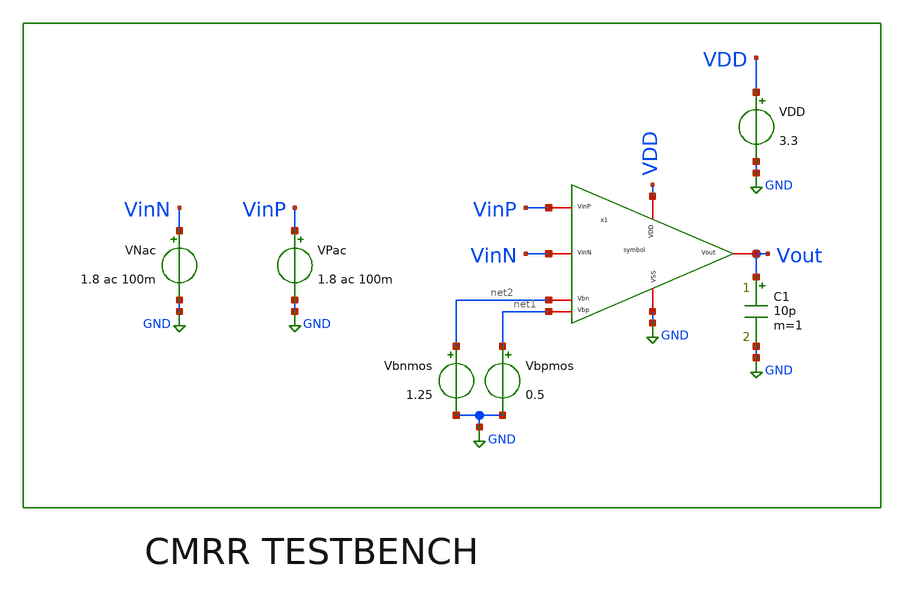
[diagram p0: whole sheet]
** sch_path: v2_bmr_bias/CMRRsim.sch
**.subckt CMRRsim
x1 VDD net1 VinP VinN Vout net2 GND symbol
VPac VinP GND 1.8 ac 100m
VNac VinN GND 1.8 ac 100m
Vbnmos net2 GND 1.25
Vbpmos net1 GND 0.5
VDD VDD GND 3.3
C1 Vout GND 10p m=1
**** begin user architecture code


.control
close all
destroy all

ac dec 20 1 500Meg
let gain_cm_db = db(Vout/VinP)
meas ac acm_dc_gain find gain_cm_db at=1

alter VNac ac = -100m
ac dec 20 1 200G
let VinDiff = v(VinP) - v(VinN)
let gain_dm_db = db(Vout/VinDiff)
meas ac adm_dc_gain find gain_dm_db at=1

let cmrr_dc   = adm_dc_gain - ac1.acm_dc_gain
let cmrr_full = gain_dm_db  - ac1.gain_cm_db

echo
echo '================ CMRR RESULTS ================'
print adm_dc_gain
print ac1.acm_dc_gain
print cmrr_dc
echo '================================================'

* --- plots ---
plot ac1.gain_cm_db gain_dm_db ylabel 'Gain (dB)' xlog title 'Common-Mode vs Differential Gain'
plot cmrr_full ylabel 'CMRR (dB)' xlog title 'CMRR vs Frequency'

.endc


**** end user architecture code
**.ends

* expanding   symbol:  /foss/designs/FOLDED/symbol.sym # of pins=7
** sym_path: v2_bmr_bias/symbol.sym
** sch_path: v2_bmr_bias/symbol.sch
.subckt symbol VDD Vbp VinP VinN Vout Vbn VSS
*.iopin Vbn
*.iopin Vbp
*.iopin VinP
*.iopin VinN
*.iopin Vout
*.iopin VDD
*.iopin VSS
XM1 net10 VinP net1 VSS sg13_hv_nmos w=7u l=1u ng=1 m=4 mm_ok=1
XM2 net9 VinN net1 VSS sg13_hv_nmos w=7u l=1u ng=1 m=4 mm_ok=1
XM3 net1 net3 VSS VSS sg13_hv_nmos w=3.75u l=1u ng=1 m=4 mm_ok=1
XM4 net10 net5 VDD VDD sg13_hv_pmos w=3.5u l=1u ng=1 m=4 mm_ok=1
XM5 net9 net5 VDD VDD sg13_hv_pmos w=3.5u l=1u ng=1 m=4 mm_ok=1
XM6 net2 Vbp net10 VDD sg13_hv_pmos w=4u l=1u ng=1 m=3 mm_ok=1
XM7 Vout Vbp net9 VDD sg13_hv_pmos w=4u l=1u ng=1 m=3 mm_ok=1
XM8 net2 Vbn net11 VSS sg13_hv_nmos w=7u l=1u ng=1 m=1 mm_ok=1
XM9 Vout Vbn net12 VSS sg13_hv_nmos w=7u l=1u ng=1 m=1 mm_ok=1
XM10 net11 net2 VSS VSS sg13_hv_nmos w=7u l=1u ng=1 m=1 mm_ok=1
XM11 net12 net2 VSS VSS sg13_hv_nmos w=7u l=1u ng=1 m=1 mm_ok=1
**** begin user architecture code



.lib cornerMOShv.lib mos_tt



**** end user architecture code
XM25 net3 net5 VDD VDD sg13_hv_pmos w=3.5u l=1u ng=1 m=1 mm_ok=1
XM12 net3 net3 VSS VSS sg13_hv_nmos w=3.75u l=1u ng=1 m=1 mm_ok=1
R1 net7 VSS 8.64k m=1
XM14 net8 net6 net7 VSS sg13_hv_nmos w=15u l=1u ng=2 m=1 mm_ok=1
XM15 net6 net6 VSS VSS sg13_hv_nmos w=3.75u l=1u ng=1 m=1 mm_ok=1
XM17 net6 net5 VDD VDD sg13_hv_pmos w=3.5u l=1u ng=1 m=1 mm_ok=1
XM18 net8 net5 VDD VDD sg13_hv_pmos w=3.5u l=1u ng=1 m=1 mm_ok=1
XM19 net4 net8 VSS VSS sg13_hv_nmos w=3.75u l=1u ng=1 m=1 mm_ok=1
XM20 net5 net6 VSS VSS sg13_hv_nmos w=3.75u l=1u ng=1 m=1 mm_ok=1
XM21 net4 net4 VDD VDD sg13_hv_pmos w=3.5u l=1u ng=1 m=1 mm_ok=1
XM22 net5 net4 VDD VDD sg13_hv_pmos w=3.5u l=1u ng=1 m=1 mm_ok=1
.ends

.GLOBAL GND
.end
